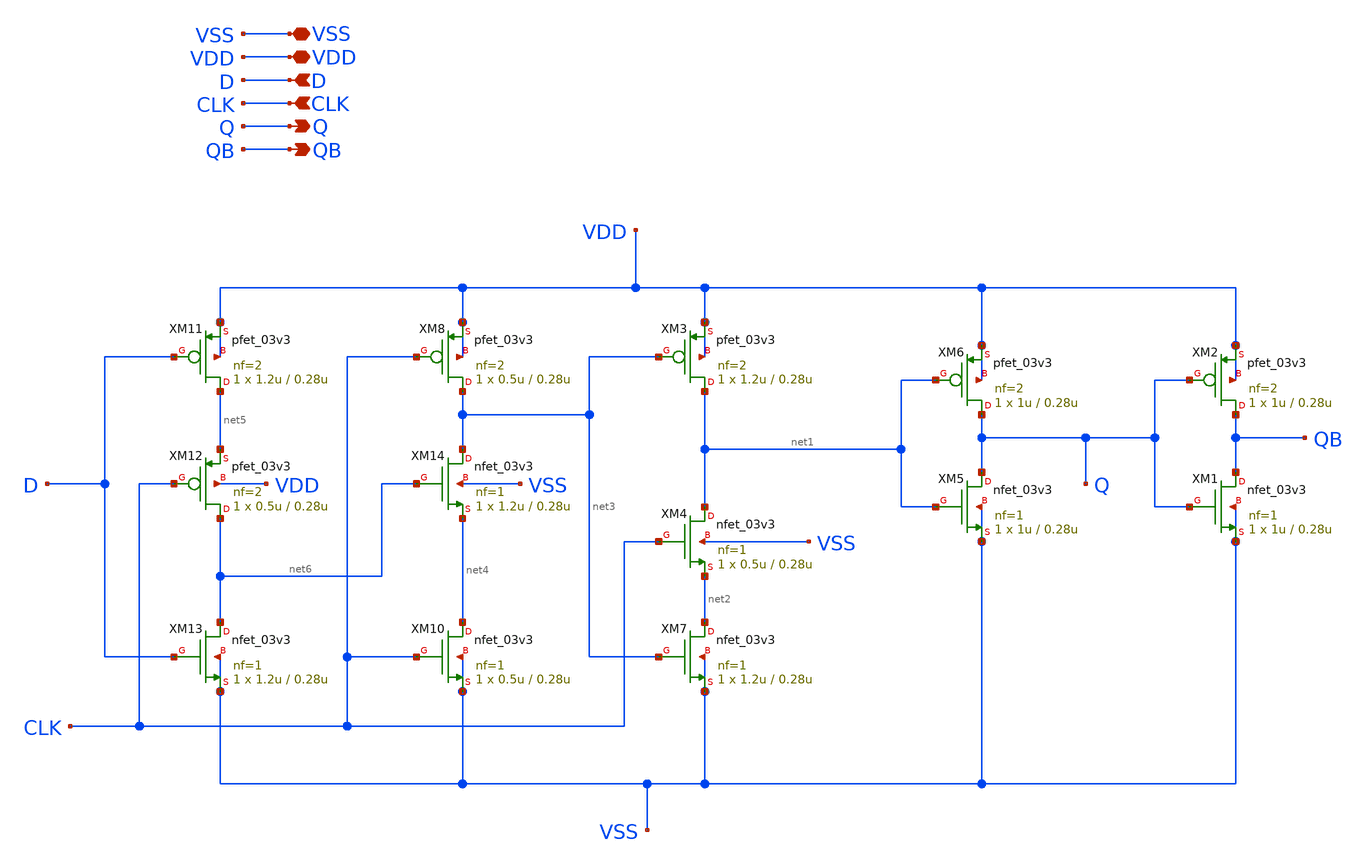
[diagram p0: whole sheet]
** sch_path: designs/libs/core_vco/vco_ffd/vco_ffd.sch
**.subckt vco_ffd Q VSS D VDD CLK QB
*.opin Q
*.iopin VSS
*.ipin D
*.iopin VDD
*.ipin CLK
*.opin QB
XM5 Q net1 VSS VSS nfet_03v3 L=0.28u W=1u nf=1 ad='int((nf+1)/2) * W/nf * 0.18u' as='int((nf+2)/2) * W/nf * 0.18u'
+ pd='2*int((nf+1)/2) * (W/nf + 0.18u)' ps='2*int((nf+2)/2) * (W/nf + 0.18u)' nrd='0.18u / W' nrs='0.18u / W'
+ sa=0 sb=0 sd=0 m=1
XM6 Q net1 VDD VDD pfet_03v3 L=0.28u W=1u nf=2 ad='int((nf+1)/2) * W/nf * 0.18u' as='int((nf+2)/2) * W/nf * 0.18u'
+ pd='2*int((nf+1)/2) * (W/nf + 0.18u)' ps='2*int((nf+2)/2) * (W/nf + 0.18u)' nrd='0.18u / W' nrs='0.18u / W'
+ sa=0 sb=0 sd=0 m=1
XM1 QB Q VSS VSS nfet_03v3 L=0.28u W=1u nf=1 ad='int((nf+1)/2) * W/nf * 0.18u' as='int((nf+2)/2) * W/nf * 0.18u'
+ pd='2*int((nf+1)/2) * (W/nf + 0.18u)' ps='2*int((nf+2)/2) * (W/nf + 0.18u)' nrd='0.18u / W' nrs='0.18u / W'
+ sa=0 sb=0 sd=0 m=1
XM2 QB Q VDD VDD pfet_03v3 L=0.28u W=1u nf=2 ad='int((nf+1)/2) * W/nf * 0.18u' as='int((nf+2)/2) * W/nf * 0.18u'
+ pd='2*int((nf+1)/2) * (W/nf + 0.18u)' ps='2*int((nf+2)/2) * (W/nf + 0.18u)' nrd='0.18u / W' nrs='0.18u / W'
+ sa=0 sb=0 sd=0 m=1
XM3 net1 net3 VDD VDD pfet_03v3 L=0.28u W=1.2u nf=2 ad='int((nf+1)/2) * W/nf * 0.18u' as='int((nf+2)/2) * W/nf * 0.18u'
+ pd='2*int((nf+1)/2) * (W/nf + 0.18u)' ps='2*int((nf+2)/2) * (W/nf + 0.18u)' nrd='0.18u / W' nrs='0.18u / W'
+ sa=0 sb=0 sd=0 m=1
XM7 net2 net3 VSS VSS nfet_03v3 L=0.28u W=1.2u nf=1 ad='int((nf+1)/2) * W/nf * 0.18u' as='int((nf+2)/2) * W/nf * 0.18u'
+ pd='2*int((nf+1)/2) * (W/nf + 0.18u)' ps='2*int((nf+2)/2) * (W/nf + 0.18u)' nrd='0.18u / W' nrs='0.18u / W'
+ sa=0 sb=0 sd=0 m=1
XM8 net3 CLK VDD VDD pfet_03v3 L=0.28u W=0.5u nf=2 ad='int((nf+1)/2) * W/nf * 0.18u' as='int((nf+2)/2) * W/nf * 0.18u'
+ pd='2*int((nf+1)/2) * (W/nf + 0.18u)' ps='2*int((nf+2)/2) * (W/nf + 0.18u)' nrd='0.18u / W' nrs='0.18u / W'
+ sa=0 sb=0 sd=0 m=1
XM10 net4 CLK VSS VSS nfet_03v3 L=0.28u W=0.5u nf=1 ad='int((nf+1)/2) * W/nf * 0.18u' as='int((nf+2)/2) * W/nf * 0.18u'
+ pd='2*int((nf+1)/2) * (W/nf + 0.18u)' ps='2*int((nf+2)/2) * (W/nf + 0.18u)' nrd='0.18u / W' nrs='0.18u / W'
+ sa=0 sb=0 sd=0 m=1
XM11 net5 D VDD VDD pfet_03v3 L=0.28u W=1.2u nf=2 ad='int((nf+1)/2) * W/nf * 0.18u' as='int((nf+2)/2) * W/nf * 0.18u'
+ pd='2*int((nf+1)/2) * (W/nf + 0.18u)' ps='2*int((nf+2)/2) * (W/nf + 0.18u)' nrd='0.18u / W' nrs='0.18u / W'
+ sa=0 sb=0 sd=0 m=1
XM12 net6 CLK net5 VDD pfet_03v3 L=0.28u W=0.5u nf=2 ad='int((nf+1)/2) * W/nf * 0.18u' as='int((nf+2)/2) * W/nf * 0.18u'
+ pd='2*int((nf+1)/2) * (W/nf + 0.18u)' ps='2*int((nf+2)/2) * (W/nf + 0.18u)' nrd='0.18u / W' nrs='0.18u / W'
+ sa=0 sb=0 sd=0 m=1
XM13 net6 D VSS VSS nfet_03v3 L=0.28u W=1.2u nf=1 ad='int((nf+1)/2) * W/nf * 0.18u' as='int((nf+2)/2) * W/nf * 0.18u'
+ pd='2*int((nf+1)/2) * (W/nf + 0.18u)' ps='2*int((nf+2)/2) * (W/nf + 0.18u)' nrd='0.18u / W' nrs='0.18u / W'
+ sa=0 sb=0 sd=0 m=1
XM14 net3 net6 net4 VSS nfet_03v3 L=0.28u W=1.2u nf=1 ad='int((nf+1)/2) * W/nf * 0.18u' as='int((nf+2)/2) * W/nf * 0.18u'
+ pd='2*int((nf+1)/2) * (W/nf + 0.18u)' ps='2*int((nf+2)/2) * (W/nf + 0.18u)' nrd='0.18u / W' nrs='0.18u / W'
+ sa=0 sb=0 sd=0 m=1
XM4 net1 CLK net2 VSS nfet_03v3 L=0.28u W=0.5u nf=1 ad='int((nf+1)/2) * W/nf * 0.18u' as='int((nf+2)/2) * W/nf * 0.18u'
+ pd='2*int((nf+1)/2) * (W/nf + 0.18u)' ps='2*int((nf+2)/2) * (W/nf + 0.18u)' nrd='0.18u / W' nrs='0.18u / W'
+ sa=0 sb=0 sd=0 m=1
**.ends
.end
